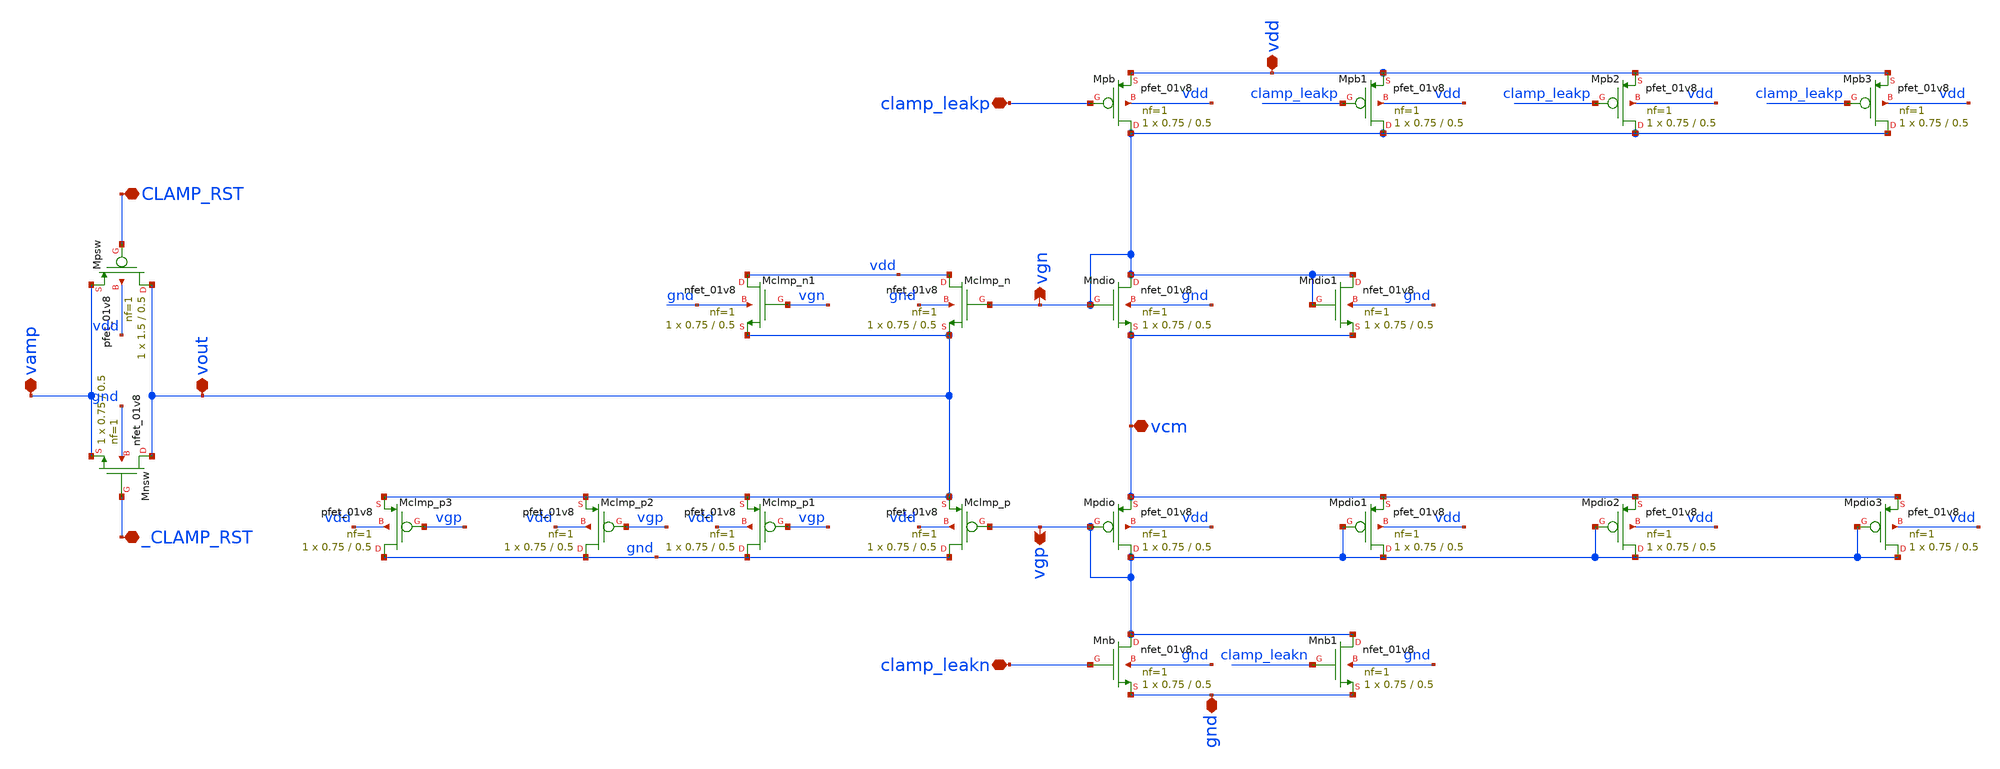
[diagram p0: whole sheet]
** sch_path: analog/xschem/col_amp_n_clamp_v1/clamp_qdvs_v2.sch
**.subckt clamp_qdvs_v2 vdd gnd vcm _CLAMP_RST CLAMP_RST clamp_leakp clamp_leakn vout vamp vgn vgp
*.iopin vdd
*.iopin gnd
*.iopin vcm
*.iopin _CLAMP_RST
*.iopin CLAMP_RST
*.iopin clamp_leakp
*.iopin clamp_leakn
*.iopin vout
*.iopin vamp
*.opin vgn
*.opin vgp
XMndio vgn vgn vcm gnd sky130_fd_pr__nfet_01v8 L=0.5 W=0.75 nf=1 ad='int((1 + 1)/2) * 0.75 / 1 * 0.29'
+ as='int((1 + 2)/2) * 0.75 / 1 * 0.29' pd='2*int((1 + 1)/2) * (0.75 / 1 + 0.29)' ps='2*int((1 + 2)/2) * (0.75 / 1 + 0.29)'
+ nrd='0.29 / 0.75 ' nrs='0.29 / 0.75 ' sa=0 sb=0 sd=0 mult=1 m=1
XMpdio vgp vgp vcm vdd sky130_fd_pr__pfet_01v8 L=0.5 W=0.75 nf=1 ad='int((1 + 1)/2) * 0.75 / 1 * 0.29'
+ as='int((1 + 2)/2) * 0.75 / 1 * 0.29' pd='2*int((1 + 1)/2) * (0.75 / 1 + 0.29)' ps='2*int((1 + 2)/2) * (0.75 / 1 + 0.29)'
+ nrd='0.29 / 0.75 ' nrs='0.29 / 0.75 ' sa=0 sb=0 sd=0 mult=1 m=1
XMpb vgn clamp_leakp vdd vdd sky130_fd_pr__pfet_01v8 L=0.5 W=0.75 nf=1 ad='int((1 + 1)/2) * 0.75 / 1 * 0.29'
+ as='int((1 + 2)/2) * 0.75 / 1 * 0.29' pd='2*int((1 + 1)/2) * (0.75 / 1 + 0.29)' ps='2*int((1 + 2)/2) * (0.75 / 1 + 0.29)'
+ nrd='0.29 / 0.75 ' nrs='0.29 / 0.75 ' sa=0 sb=0 sd=0 mult=1 m=1
XMnb vgp clamp_leakn gnd gnd sky130_fd_pr__nfet_01v8 L=0.5 W=0.75 nf=1 ad='int((1 + 1)/2) * 0.75 / 1 * 0.29'
+ as='int((1 + 2)/2) * 0.75 / 1 * 0.29' pd='2*int((1 + 1)/2) * (0.75 / 1 + 0.29)' ps='2*int((1 + 2)/2) * (0.75 / 1 + 0.29)'
+ nrd='0.29 / 0.75 ' nrs='0.29 / 0.75 ' sa=0 sb=0 sd=0 mult=1 m=1
XMclmp_n vdd vgn vout gnd sky130_fd_pr__nfet_01v8 L=0.5 W=0.75 nf=1 ad='int((1 + 1)/2) * 0.75 / 1 * 0.29'
+ as='int((1 + 2)/2) * 0.75 / 1 * 0.29' pd='2*int((1 + 1)/2) * (0.75 / 1 + 0.29)' ps='2*int((1 + 2)/2) * (0.75 / 1 + 0.29)'
+ nrd='0.29 / 0.75 ' nrs='0.29 / 0.75 ' sa=0 sb=0 sd=0 mult=1 m=1
XMclmp_p gnd vgp vout vdd sky130_fd_pr__pfet_01v8 L=0.5 W=0.75 nf=1 ad='int((1 + 1)/2) * 0.75 / 1 * 0.29'
+ as='int((1 + 2)/2) * 0.75 / 1 * 0.29' pd='2*int((1 + 1)/2) * (0.75 / 1 + 0.29)' ps='2*int((1 + 2)/2) * (0.75 / 1 + 0.29)'
+ nrd='0.29 / 0.75 ' nrs='0.29 / 0.75 ' sa=0 sb=0 sd=0 mult=1 m=1
XMnsw vout _CLAMP_RST vamp gnd sky130_fd_pr__nfet_01v8 L=0.5 W=0.75 nf=1 ad='int((1 + 1)/2) * 0.75 / 1 * 0.29'
+ as='int((1 + 2)/2) * 0.75 / 1 * 0.29' pd='2*int((1 + 1)/2) * (0.75 / 1 + 0.29)' ps='2*int((1 + 2)/2) * (0.75 / 1 + 0.29)'
+ nrd='0.29 / 0.75 ' nrs='0.29 / 0.75 ' sa=0 sb=0 sd=0 mult=1 m=1
XMpsw vout CLAMP_RST vamp vdd sky130_fd_pr__pfet_01v8 L=0.5 W=1.5 nf=1 ad='int((1 + 1)/2) * 1.5 / 1 * 0.29'
+ as='int((1 + 2)/2) * 1.5 / 1 * 0.29' pd='2*int((1 + 1)/2) * (1.5 / 1 + 0.29)' ps='2*int((1 + 2)/2) * (1.5 / 1 + 0.29)'
+ nrd='0.29 / 1.5 ' nrs='0.29 / 1.5 ' sa=0 sb=0 sd=0 mult=1 m=1
XMclmp_p1 gnd vgp vout vdd sky130_fd_pr__pfet_01v8 L=0.5 W=0.75 nf=1 ad='int((1 + 1)/2) * 0.75 / 1 * 0.29'
+ as='int((1 + 2)/2) * 0.75 / 1 * 0.29' pd='2*int((1 + 1)/2) * (0.75 / 1 + 0.29)' ps='2*int((1 + 2)/2) * (0.75 / 1 + 0.29)'
+ nrd='0.29 / 0.75 ' nrs='0.29 / 0.75 ' sa=0 sb=0 sd=0 mult=1 m=1
XMclmp_p2 gnd vgp vout vdd sky130_fd_pr__pfet_01v8 L=0.5 W=0.75 nf=1 ad='int((1 + 1)/2) * 0.75 / 1 * 0.29'
+ as='int((1 + 2)/2) * 0.75 / 1 * 0.29' pd='2*int((1 + 1)/2) * (0.75 / 1 + 0.29)' ps='2*int((1 + 2)/2) * (0.75 / 1 + 0.29)'
+ nrd='0.29 / 0.75 ' nrs='0.29 / 0.75 ' sa=0 sb=0 sd=0 mult=1 m=1
XMclmp_p3 gnd vgp vout vdd sky130_fd_pr__pfet_01v8 L=0.5 W=0.75 nf=1 ad='int((1 + 1)/2) * 0.75 / 1 * 0.29'
+ as='int((1 + 2)/2) * 0.75 / 1 * 0.29' pd='2*int((1 + 1)/2) * (0.75 / 1 + 0.29)' ps='2*int((1 + 2)/2) * (0.75 / 1 + 0.29)'
+ nrd='0.29 / 0.75 ' nrs='0.29 / 0.75 ' sa=0 sb=0 sd=0 mult=1 m=1
XMnb1 vgp clamp_leakn gnd gnd sky130_fd_pr__nfet_01v8 L=0.5 W=0.75 nf=1 ad='int((1 + 1)/2) * 0.75 / 1 * 0.29'
+ as='int((1 + 2)/2) * 0.75 / 1 * 0.29' pd='2*int((1 + 1)/2) * (0.75 / 1 + 0.29)' ps='2*int((1 + 2)/2) * (0.75 / 1 + 0.29)'
+ nrd='0.29 / 0.75 ' nrs='0.29 / 0.75 ' sa=0 sb=0 sd=0 mult=1 m=1
XMpb1 vgn clamp_leakp vdd vdd sky130_fd_pr__pfet_01v8 L=0.5 W=0.75 nf=1 ad='int((1 + 1)/2) * 0.75 / 1 * 0.29'
+ as='int((1 + 2)/2) * 0.75 / 1 * 0.29' pd='2*int((1 + 1)/2) * (0.75 / 1 + 0.29)' ps='2*int((1 + 2)/2) * (0.75 / 1 + 0.29)'
+ nrd='0.29 / 0.75 ' nrs='0.29 / 0.75 ' sa=0 sb=0 sd=0 mult=1 m=1
XMpdio1 vgp vgp vcm vdd sky130_fd_pr__pfet_01v8 L=0.5 W=0.75 nf=1 ad='int((1 + 1)/2) * 0.75 / 1 * 0.29'
+ as='int((1 + 2)/2) * 0.75 / 1 * 0.29' pd='2*int((1 + 1)/2) * (0.75 / 1 + 0.29)' ps='2*int((1 + 2)/2) * (0.75 / 1 + 0.29)'
+ nrd='0.29 / 0.75 ' nrs='0.29 / 0.75 ' sa=0 sb=0 sd=0 mult=1 m=1
XMpdio2 vgp vgp vcm vdd sky130_fd_pr__pfet_01v8 L=0.5 W=0.75 nf=1 ad='int((1 + 1)/2) * 0.75 / 1 * 0.29'
+ as='int((1 + 2)/2) * 0.75 / 1 * 0.29' pd='2*int((1 + 1)/2) * (0.75 / 1 + 0.29)' ps='2*int((1 + 2)/2) * (0.75 / 1 + 0.29)'
+ nrd='0.29 / 0.75 ' nrs='0.29 / 0.75 ' sa=0 sb=0 sd=0 mult=1 m=1
XMpdio3 vgp vgp vcm vdd sky130_fd_pr__pfet_01v8 L=0.5 W=0.75 nf=1 ad='int((1 + 1)/2) * 0.75 / 1 * 0.29'
+ as='int((1 + 2)/2) * 0.75 / 1 * 0.29' pd='2*int((1 + 1)/2) * (0.75 / 1 + 0.29)' ps='2*int((1 + 2)/2) * (0.75 / 1 + 0.29)'
+ nrd='0.29 / 0.75 ' nrs='0.29 / 0.75 ' sa=0 sb=0 sd=0 mult=1 m=1
XMndio1 vgn vgn vcm gnd sky130_fd_pr__nfet_01v8 L=0.5 W=0.75 nf=1 ad='int((1 + 1)/2) * 0.75 / 1 * 0.29'
+ as='int((1 + 2)/2) * 0.75 / 1 * 0.29' pd='2*int((1 + 1)/2) * (0.75 / 1 + 0.29)' ps='2*int((1 + 2)/2) * (0.75 / 1 + 0.29)'
+ nrd='0.29 / 0.75 ' nrs='0.29 / 0.75 ' sa=0 sb=0 sd=0 mult=1 m=1
XMclmp_n1 vdd vgn vout gnd sky130_fd_pr__nfet_01v8 L=0.5 W=0.75 nf=1 ad='int((1 + 1)/2) * 0.75 / 1 * 0.29'
+ as='int((1 + 2)/2) * 0.75 / 1 * 0.29' pd='2*int((1 + 1)/2) * (0.75 / 1 + 0.29)' ps='2*int((1 + 2)/2) * (0.75 / 1 + 0.29)'
+ nrd='0.29 / 0.75 ' nrs='0.29 / 0.75 ' sa=0 sb=0 sd=0 mult=1 m=1
XMpb2 vgn clamp_leakp vdd vdd sky130_fd_pr__pfet_01v8 L=0.5 W=0.75 nf=1 ad='int((1 + 1)/2) * 0.75 / 1 * 0.29'
+ as='int((1 + 2)/2) * 0.75 / 1 * 0.29' pd='2*int((1 + 1)/2) * (0.75 / 1 + 0.29)' ps='2*int((1 + 2)/2) * (0.75 / 1 + 0.29)'
+ nrd='0.29 / 0.75 ' nrs='0.29 / 0.75 ' sa=0 sb=0 sd=0 mult=1 m=1
XMpb3 vgn clamp_leakp vdd vdd sky130_fd_pr__pfet_01v8 L=0.5 W=0.75 nf=1 ad='int((1 + 1)/2) * 0.75 / 1 * 0.29'
+ as='int((1 + 2)/2) * 0.75 / 1 * 0.29' pd='2*int((1 + 1)/2) * (0.75 / 1 + 0.29)' ps='2*int((1 + 2)/2) * (0.75 / 1 + 0.29)'
+ nrd='0.29 / 0.75 ' nrs='0.29 / 0.75 ' sa=0 sb=0 sd=0 mult=1 m=1
**.ends
.end
